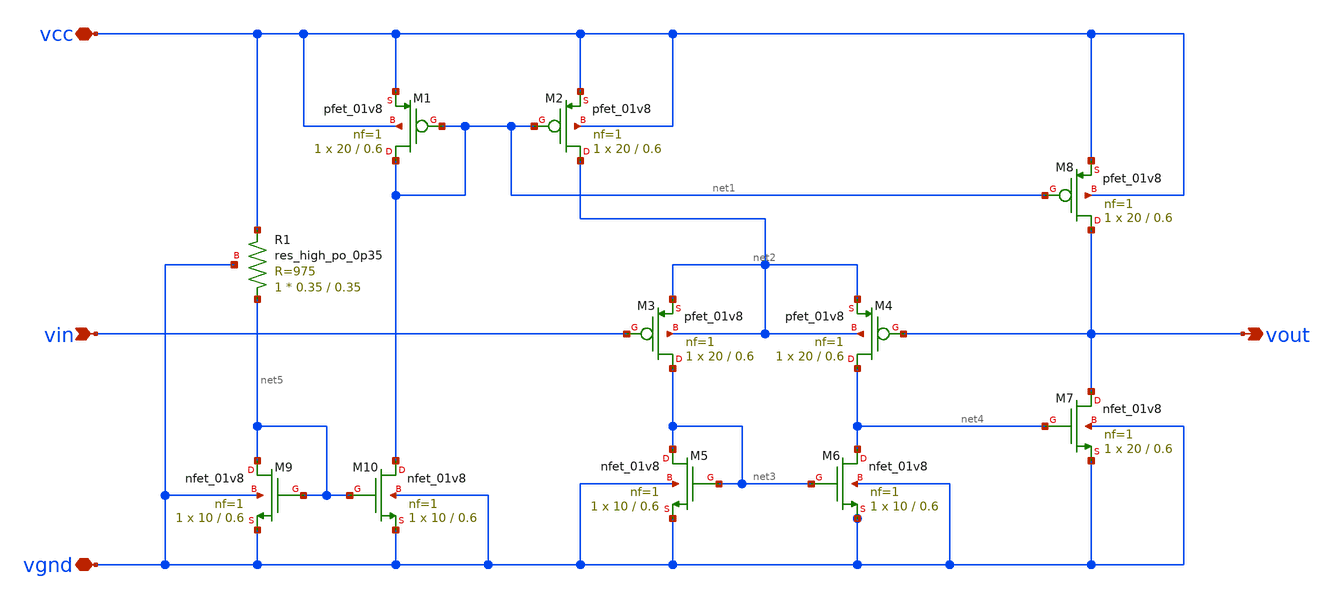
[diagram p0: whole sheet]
** sch_path: xschem/a2_opamp.sch
**.subckt a2_opamp vin vcc vgnd vout
*.ipin vin
*.iopin vcc
*.iopin vgnd
*.opin vout
XM1 net1 net1 vcc vcc sky130_fd_pr__pfet_01v8 L=0.6 W=20 nf=1 ad='int((nf+1)/2) * W/nf * 0.29' as='int((nf+2)/2) * W/nf * 0.29'
+ pd='2*int((nf+1)/2) * (W/nf + 0.29)' ps='2*int((nf+2)/2) * (W/nf + 0.29)' nrd='0.29 / W' nrs='0.29 / W'
+ sa=0 sb=0 sd=0 mult=1 m=1
XM2 net2 net1 vcc vcc sky130_fd_pr__pfet_01v8 L=0.6 W=20 nf=1 ad='int((nf+1)/2) * W/nf * 0.29' as='int((nf+2)/2) * W/nf * 0.29'
+ pd='2*int((nf+1)/2) * (W/nf + 0.29)' ps='2*int((nf+2)/2) * (W/nf + 0.29)' nrd='0.29 / W' nrs='0.29 / W'
+ sa=0 sb=0 sd=0 mult=1 m=1
XM3 net3 vin net2 net2 sky130_fd_pr__pfet_01v8 L=0.6 W=20 nf=1 ad='int((nf+1)/2) * W/nf * 0.29' as='int((nf+2)/2) * W/nf * 0.29'
+ pd='2*int((nf+1)/2) * (W/nf + 0.29)' ps='2*int((nf+2)/2) * (W/nf + 0.29)' nrd='0.29 / W' nrs='0.29 / W'
+ sa=0 sb=0 sd=0 mult=1 m=1
XM4 net4 vout net2 net2 sky130_fd_pr__pfet_01v8 L=0.6 W=20 nf=1 ad='int((nf+1)/2) * W/nf * 0.29' as='int((nf+2)/2) * W/nf * 0.29'
+ pd='2*int((nf+1)/2) * (W/nf + 0.29)' ps='2*int((nf+2)/2) * (W/nf + 0.29)' nrd='0.29 / W' nrs='0.29 / W'
+ sa=0 sb=0 sd=0 mult=1 m=1
XM5 net3 net3 vgnd vgnd sky130_fd_pr__nfet_01v8 L=0.6 W=10 nf=1 ad='int((nf+1)/2) * W/nf * 0.29' as='int((nf+2)/2) * W/nf * 0.29'
+ pd='2*int((nf+1)/2) * (W/nf + 0.29)' ps='2*int((nf+2)/2) * (W/nf + 0.29)' nrd='0.29 / W' nrs='0.29 / W'
+ sa=0 sb=0 sd=0 mult=1 m=1
XM6 net4 net3 vgnd vgnd sky130_fd_pr__nfet_01v8 L=0.6 W=10 nf=1 ad='int((nf+1)/2) * W/nf * 0.29' as='int((nf+2)/2) * W/nf * 0.29'
+ pd='2*int((nf+1)/2) * (W/nf + 0.29)' ps='2*int((nf+2)/2) * (W/nf + 0.29)' nrd='0.29 / W' nrs='0.29 / W'
+ sa=0 sb=0 sd=0 mult=1 m=1
XM7 vout net4 vgnd vgnd sky130_fd_pr__nfet_01v8 L=0.6 W=20 nf=1 ad='int((nf+1)/2) * W/nf * 0.29' as='int((nf+2)/2) * W/nf * 0.29'
+ pd='2*int((nf+1)/2) * (W/nf + 0.29)' ps='2*int((nf+2)/2) * (W/nf + 0.29)' nrd='0.29 / W' nrs='0.29 / W'
+ sa=0 sb=0 sd=0 mult=1 m=1
XM8 vout net1 vcc vcc sky130_fd_pr__pfet_01v8 L=0.6 W=20 nf=1 ad='int((nf+1)/2) * W/nf * 0.29' as='int((nf+2)/2) * W/nf * 0.29'
+ pd='2*int((nf+1)/2) * (W/nf + 0.29)' ps='2*int((nf+2)/2) * (W/nf + 0.29)' nrd='0.29 / W' nrs='0.29 / W'
+ sa=0 sb=0 sd=0 mult=1 m=1
XM9 net5 net5 vgnd vgnd sky130_fd_pr__nfet_01v8 L=0.6 W=10 nf=1 ad='int((nf+1)/2) * W/nf * 0.29' as='int((nf+2)/2) * W/nf * 0.29'
+ pd='2*int((nf+1)/2) * (W/nf + 0.29)' ps='2*int((nf+2)/2) * (W/nf + 0.29)' nrd='0.29 / W' nrs='0.29 / W'
+ sa=0 sb=0 sd=0 mult=1 m=1
XM10 net1 net5 vgnd vgnd sky130_fd_pr__nfet_01v8 L=0.6 W=10 nf=1 ad='int((nf+1)/2) * W/nf * 0.29' as='int((nf+2)/2) * W/nf * 0.29'
+ pd='2*int((nf+1)/2) * (W/nf + 0.29)' ps='2*int((nf+2)/2) * (W/nf + 0.29)' nrd='0.29 / W' nrs='0.29 / W'
+ sa=0 sb=0 sd=0 mult=1 m=1
XR1 net5 vcc vgnd sky130_fd_pr__res_high_po_0p35 L=0.35 mult=1 m=1
**.ends
.end
